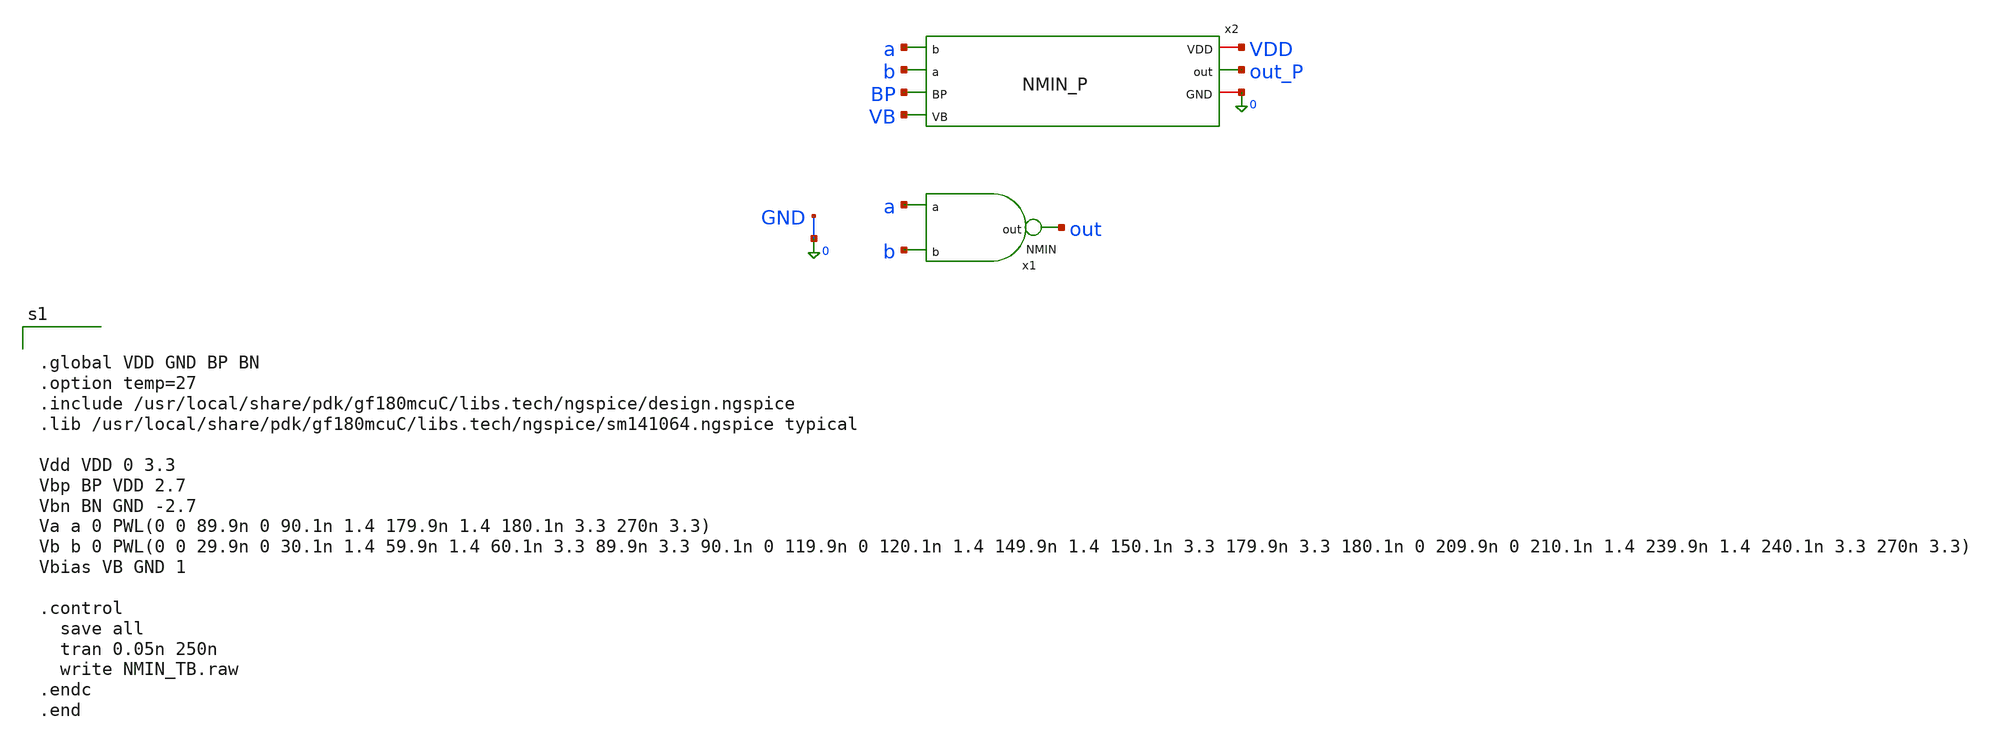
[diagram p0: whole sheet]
** sch_path: xschem_designs/NMIN_TB.sch
**.subckt NMIN_TB
x1 out a b NMIN
x2 a VDD b BP out_P VB 0 NMIN_P
**** begin user architecture code


.global VDD GND BP BN
.option temp=27
.include /usr/local/share/pdk/gf180mcuC/libs.tech/ngspice/design.ngspice
.lib /usr/local/share/pdk/gf180mcuC/libs.tech/ngspice/sm141064.ngspice typical

Vdd VDD 0 3.3
Vbp BP VDD 2.7
Vbn BN GND -2.7
Va a 0 PWL(0 0 89.9n 0 90.1n 1.4 179.9n 1.4 180.1n 3.3 270n 3.3)
Vb b 0 PWL(0 0 29.9n 0 30.1n 1.4 59.9n 1.4 60.1n 3.3 89.9n 3.3 90.1n 0 119.9n 0 120.1n 1.4 149.9n
+ 1.4 150.1n 3.3 179.9n 3.3 180.1n 0 209.9n 0 210.1n 1.4 239.9n 1.4 240.1n 3.3 270n 3.3)
Vbias VB GND 1

.control
  save all
  tran 0.05n 250n
  write NMIN_TB.raw
.endc
.end


**** end user architecture code
**.ends

* expanding   symbol:  xschem_designs/NMIN.sym # of pins=3
** sym_path: xschem_designs/NMIN.sym
** sch_path: xschem_designs/NMIN.sch
.subckt NMIN out a b
*.ipin a
*.ipin b
*.opin out
XM21 net1 a VDD VDD pfet_03v3 L=0.28u W=0.44u nf=1 ad='int((nf+1)/2) * W/nf * 0.18u' as='int((nf+2)/2) * W/nf * 0.18u'
+ pd='2*int((nf+1)/2) * (W/nf + 0.18u)' ps='2*int((nf+2)/2) * (W/nf + 0.18u)' nrd='0.18u / W' nrs='0.18u / W'
+ sa=0 sb=0 sd=0 m=1 par=1
XM22 out out net1 VDD pfet_03v3 L=1.12u W=0.22u nf=1 ad='int((nf+1)/2) * W/nf * 0.18u' as='int((nf+2)/2) * W/nf * 0.18u'
+ pd='2*int((nf+1)/2) * (W/nf + 0.18u)' ps='2*int((nf+2)/2) * (W/nf + 0.18u)' nrd='0.18u / W' nrs='0.18u / W'
+ sa=0 sb=0 sd=0 m=1 par=1
XM23 out a VDD BP pfet_06v0 L=1.1u W=0.60u nf=1 ad='int((nf+1)/2) * W/nf * 0.18u' as='int((nf+2)/2) * W/nf * 0.18u'
+ pd='2*int((nf+1)/2) * (W/nf + 0.18u)' ps='2*int((nf+2)/2) * (W/nf + 0.18u)' nrd='0.18u / W' nrs='0.18u / W'
+ sa=0 sb=0 sd=0 m=1 par=1
XM24 out b VDD BP pfet_06v0 L=1.1u W=0.60u nf=1 ad='int((nf+1)/2) * W/nf * 0.18u' as='int((nf+2)/2) * W/nf * 0.18u'
+ pd='2*int((nf+1)/2) * (W/nf + 0.18u)' ps='2*int((nf+2)/2) * (W/nf + 0.18u)' nrd='0.18u / W' nrs='0.18u / W'
+ sa=0 sb=0 sd=0 m=1 par=1
XM25 net1 b VDD VDD pfet_03v3 L=0.28u W=0.44u nf=1 ad='int((nf+1)/2) * W/nf * 0.18u' as='int((nf+2)/2) * W/nf * 0.18u'
+ pd='2*int((nf+1)/2) * (W/nf + 0.18u)' ps='2*int((nf+2)/2) * (W/nf + 0.18u)' nrd='0.18u / W' nrs='0.18u / W'
+ sa=0 sb=0 sd=0 m=1 par=1
XM26 out out net2 GND nfet_03v3 L=2.24u W=0.22u nf=1 ad='int((nf+1)/2) * W/nf * 0.18u' as='int((nf+2)/2) * W/nf * 0.18u'
+ pd='2*int((nf+1)/2) * (W/nf + 0.18u)' ps='2*int((nf+2)/2) * (W/nf + 0.18u)' nrd='0.18u / W' nrs='0.18u / W'
+ sa=0 sb=0 sd=0 m=1 par=1
XM27 net3 a GND BN nfet_06v0 L=1.4u W=0.30u nf=1 ad='int((nf+1)/2) * W/nf * 0.18u' as='int((nf+2)/2) * W/nf * 0.18u'
+ pd='2*int((nf+1)/2) * (W/nf + 0.18u)' ps='2*int((nf+2)/2) * (W/nf + 0.18u)' nrd='0.18u / W' nrs='0.18u / W'
+ sa=0 sb=0 sd=0 m=1 par=1
XM28 out b net3 BN nfet_06v0 L=1.4u W=0.30u nf=1 ad='int((nf+1)/2) * W/nf * 0.18u' as='int((nf+2)/2) * W/nf * 0.18u'
+ pd='2*int((nf+1)/2) * (W/nf + 0.18u)' ps='2*int((nf+2)/2) * (W/nf + 0.18u)' nrd='0.18u / W' nrs='0.18u / W'
+ sa=0 sb=0 sd=0 m=1 par=1
XM29 net4 a GND GND nfet_03v3 L=0.28u W=0.22u nf=1 ad='int((nf+1)/2) * W/nf * 0.18u' as='int((nf+2)/2) * W/nf * 0.18u'
+ pd='2*int((nf+1)/2) * (W/nf + 0.18u)' ps='2*int((nf+2)/2) * (W/nf + 0.18u)' nrd='0.18u / W' nrs='0.18u / W'
+ sa=0 sb=0 sd=0 m=1 par=1
XM30 net2 b net4 GND nfet_03v3 L=0.28u W=0.22u nf=1 ad='int((nf+1)/2) * W/nf * 0.18u' as='int((nf+2)/2) * W/nf * 0.18u'
+ pd='2*int((nf+1)/2) * (W/nf + 0.18u)' ps='2*int((nf+2)/2) * (W/nf + 0.18u)' nrd='0.18u / W' nrs='0.18u / W'
+ sa=0 sb=0 sd=0 m=1 par=1
.ends


* expanding   symbol:  xschem_designs/NMIN_P.sym # of pins=7
** sym_path: xschem_designs/NMIN_P.sym
** sch_path: xschem_designs/NMIN_P.sch
.subckt NMIN_P b VDD a BP out VB GND
*.ipin a
*.opin out
*.iopin GND
*.iopin VDD
*.ipin BP
*.ipin VB
*.ipin b
XM1 out VB GND GND nfet_03v3 L=1.12u W=0.22u nf=1 ad='int((nf+1)/2) * W/nf * 0.18u' as='int((nf+2)/2) * W/nf * 0.18u'
+ pd='2*int((nf+1)/2) * (W/nf + 0.18u)' ps='2*int((nf+2)/2) * (W/nf + 0.18u)' nrd='0.18u / W' nrs='0.18u / W'
+ sa=0 sb=0 sd=0 m=1 par=1
XM2 net1 b VDD VDD pfet_03v3 L=0.28u W=0.44u nf=1 ad='int((nf+1)/2) * W/nf * 0.18u' as='int((nf+2)/2) * W/nf * 0.18u'
+ pd='2*int((nf+1)/2) * (W/nf + 0.18u)' ps='2*int((nf+2)/2) * (W/nf + 0.18u)' nrd='0.18u / W' nrs='0.18u / W'
+ sa=0 sb=0 sd=0 m=1 par=1
XM3 out a VDD BP pfet_06v0 L=1.1u W=0.30u nf=1 ad='int((nf+1)/2) * W/nf * 0.18u' as='int((nf+2)/2) * W/nf * 0.18u'
+ pd='2*int((nf+1)/2) * (W/nf + 0.18u)' ps='2*int((nf+2)/2) * (W/nf + 0.18u)' nrd='0.18u / W' nrs='0.18u / W'
+ sa=0 sb=0 sd=0 m=1
XM4 out out net1 VDD pfet_03v3 L=1.12u W=0.22u nf=1 ad='int((nf+1)/2) * W/nf * 0.18u' as='int((nf+2)/2) * W/nf * 0.18u'
+ pd='2*int((nf+1)/2) * (W/nf + 0.18u)' ps='2*int((nf+2)/2) * (W/nf + 0.18u)' nrd='0.18u / W' nrs='0.18u / W'
+ sa=0 sb=0 sd=0 m=1 par=1
XM9 out b VDD BP pfet_06v0 L=1.1u W=0.30u nf=1 ad='int((nf+1)/2) * W/nf * 0.18u' as='int((nf+2)/2) * W/nf * 0.18u'
+ pd='2*int((nf+1)/2) * (W/nf + 0.18u)' ps='2*int((nf+2)/2) * (W/nf + 0.18u)' nrd='0.18u / W' nrs='0.18u / W'
+ sa=0 sb=0 sd=0 m=1
XM10 net1 a VDD VDD pfet_03v3 L=0.28u W=0.44u nf=1 ad='int((nf+1)/2) * W/nf * 0.18u' as='int((nf+2)/2) * W/nf * 0.18u'
+ pd='2*int((nf+1)/2) * (W/nf + 0.18u)' ps='2*int((nf+2)/2) * (W/nf + 0.18u)' nrd='0.18u / W' nrs='0.18u / W'
+ sa=0 sb=0 sd=0 m=1 par=1
.ends

.end
